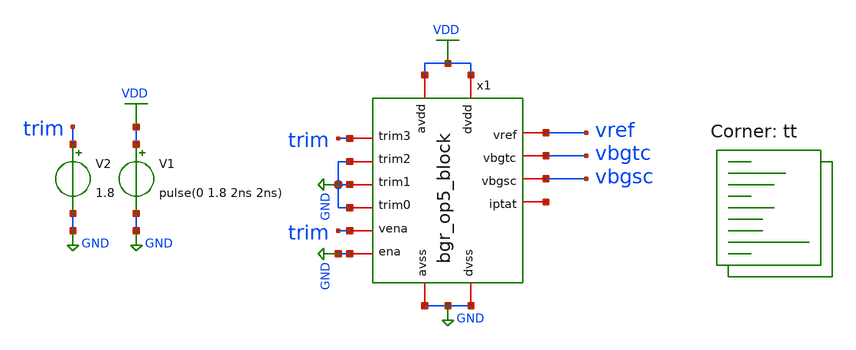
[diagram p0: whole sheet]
** sch_path: xschem/bgr_op5_block_Startup_tb_TT.sch
**.subckt bgr_op5_block_Startup_tb_TT
V1 VDD GND pulse(0 1.8 2ns 2ns)
V2 trim GND 1.8
x1 net1 VDD vbgtc GND trim vbgsc GND GND GND trim GND VDD GND vref bgr_op5_block
**** begin user architecture code


.include ~/chipalooza/sky130_gff_ip__bgr_1.2v/magic/bgr_op5_block_rev1.pex.spice
.option savecurrents
.control
save all
op
remzerovec
write bgr_op5_block_tb.raw

set appendwrite
set wr_singlescale
set wr_vecnames
option numdgt=3

****Power****
tran 10us 50ms
*write bgr_op5_tb.raw
write Startup_TT.raw vref vdd
set altshow
show >> bgr_op5.lis
remzerovec
meas tran ave_v avg vdd
meas tran ave_i avg i(v1)
let ave_power='ave_v*(-ave_i)
plot vdd vref
plot vg1 vgstart start
*plot -i(v1)
print ave_power

.endc


.lib $::SKYWATER_MODELS/sky130.lib.spice tt
**** end user architecture code
**.ends
.GLOBAL GND
.GLOBAL VDD
.end
